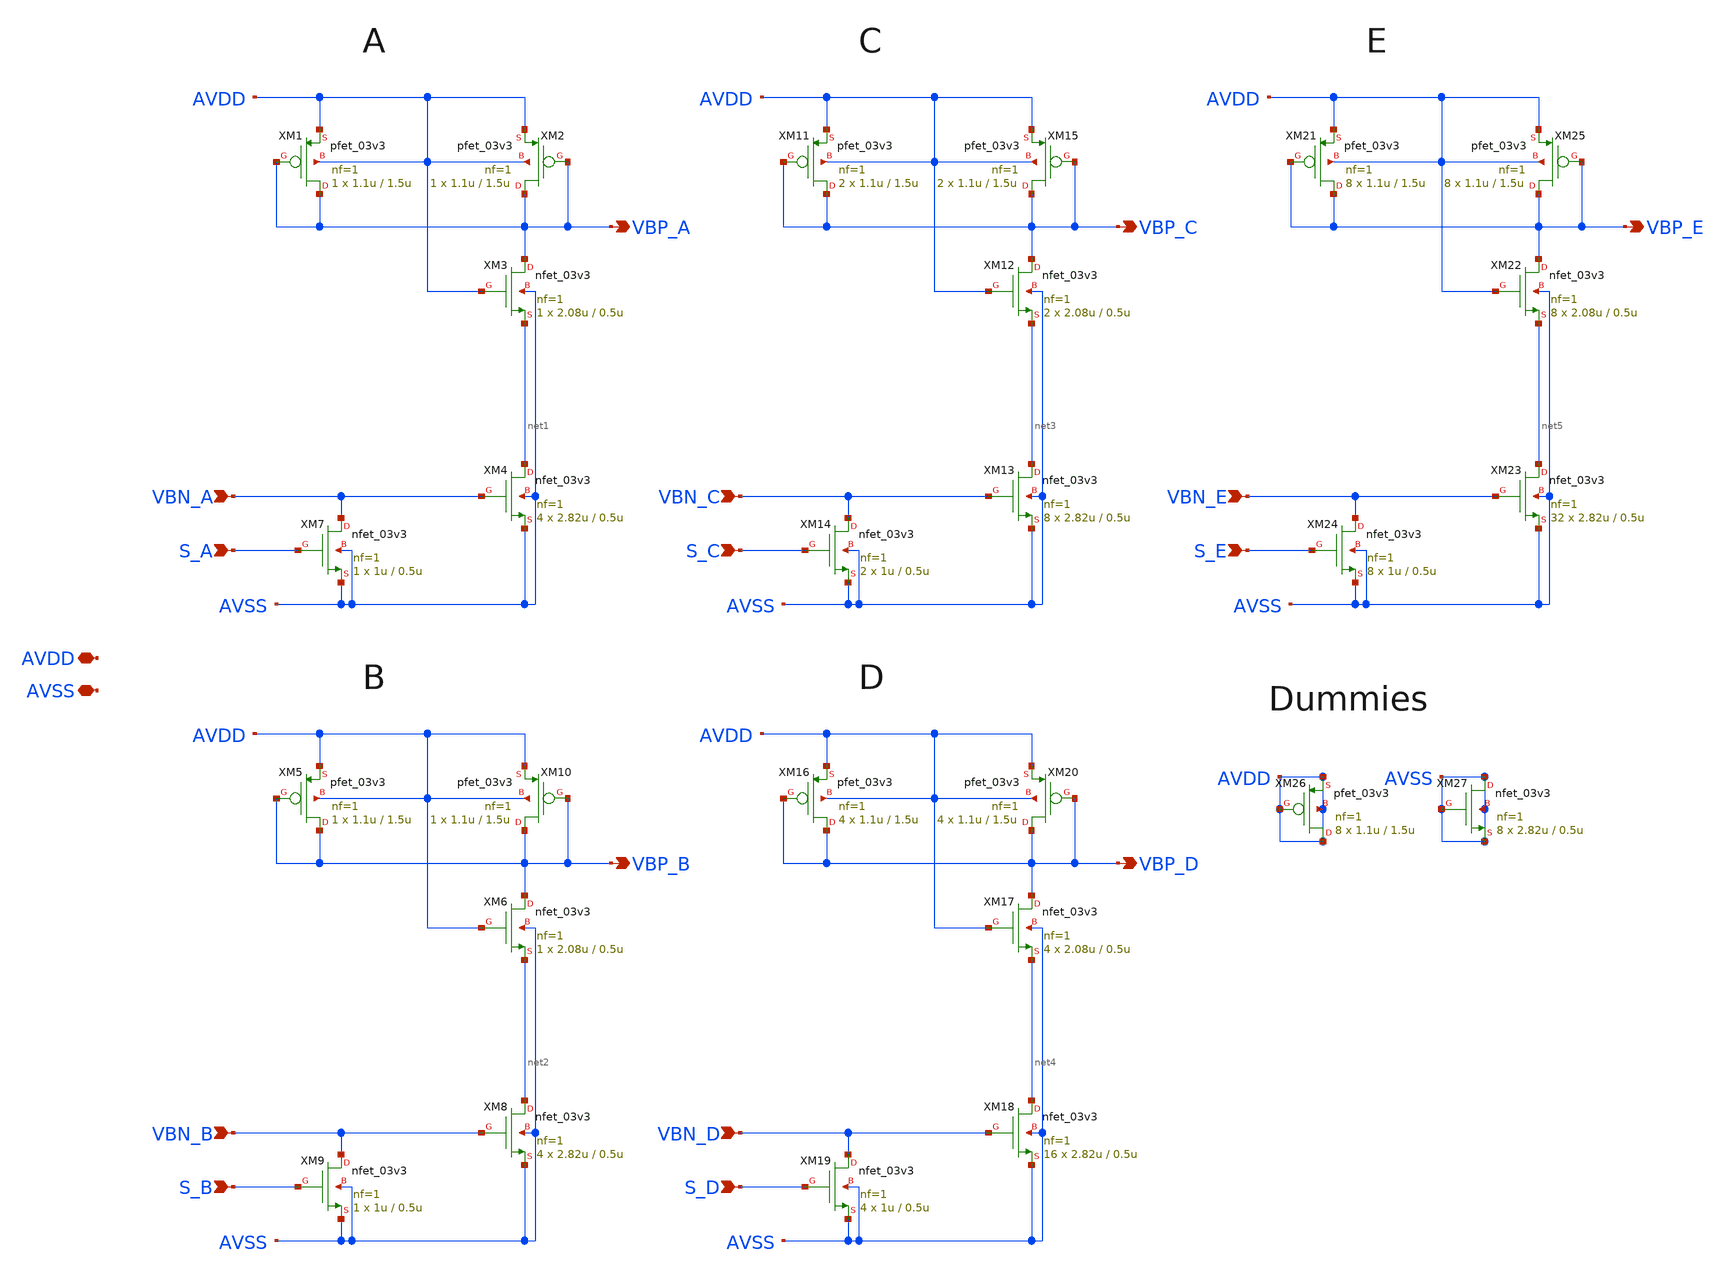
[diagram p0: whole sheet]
** sch_path: designs/libs/core_analog/feed_forward_zero/feed_forward_zero_v2_merged.sch
**.subckt feed_forward_zero_v2_merged VBP_E AVDD VBN_A VBP_A VBN_B S_B VBP_B VBN_C S_C VBP_C VBN_D
*+ S_D VBP_D VBN_E S_E S_A AVSS
*.opin VBP_E
*.iopin AVDD
*.ipin VBN_A
*.opin VBP_A
*.ipin VBN_B
*.ipin S_B
*.opin VBP_B
*.ipin VBN_C
*.ipin S_C
*.opin VBP_C
*.ipin VBN_D
*.ipin S_D
*.opin VBP_D
*.ipin VBN_E
*.ipin S_E
*.ipin S_A
*.iopin AVSS
XM1 VBP_A VBP_A AVDD AVDD pfet_03v3 L=1.5u W=1.1u nf=1 ad='int((nf+1)/2) * W/nf * 0.18u' as='int((nf+2)/2) * W/nf * 0.18u'
+ pd='2*int((nf+1)/2) * (W/nf + 0.18u)' ps='2*int((nf+2)/2) * (W/nf + 0.18u)' nrd='0.18u / W' nrs='0.18u / W'
+ sa=0 sb=0 sd=0 m=1
XM3 VBP_A AVDD net1 AVSS nfet_03v3 L=0.5u W=2.08u nf=1 ad='int((nf+1)/2) * W/nf * 0.18u' as='int((nf+2)/2) * W/nf * 0.18u'
+ pd='2*int((nf+1)/2) * (W/nf + 0.18u)' ps='2*int((nf+2)/2) * (W/nf + 0.18u)' nrd='0.18u / W' nrs='0.18u / W'
+ sa=0 sb=0 sd=0 m=1
XM4 net1 VBN_A AVSS AVSS nfet_03v3 L=0.5u W=2.82u nf=1 ad='int((nf+1)/2) * W/nf * 0.18u' as='int((nf+2)/2) * W/nf * 0.18u'
+ pd='2*int((nf+1)/2) * (W/nf + 0.18u)' ps='2*int((nf+2)/2) * (W/nf + 0.18u)' nrd='0.18u / W' nrs='0.18u / W'
+ sa=0 sb=0 sd=0 m=4
XM7 VBN_A S_A AVSS AVSS nfet_03v3 L=0.5u W=1u nf=1 ad='int((nf+1)/2) * W/nf * 0.18u' as='int((nf+2)/2) * W/nf * 0.18u'
+ pd='2*int((nf+1)/2) * (W/nf + 0.18u)' ps='2*int((nf+2)/2) * (W/nf + 0.18u)' nrd='0.18u / W' nrs='0.18u / W'
+ sa=0 sb=0 sd=0 m=1
XM2 VBP_A VBP_A AVDD AVDD pfet_03v3 L=1.5u W=1.1u nf=1 ad='int((nf+1)/2) * W/nf * 0.18u' as='int((nf+2)/2) * W/nf * 0.18u'
+ pd='2*int((nf+1)/2) * (W/nf + 0.18u)' ps='2*int((nf+2)/2) * (W/nf + 0.18u)' nrd='0.18u / W' nrs='0.18u / W'
+ sa=0 sb=0 sd=0 m=1
XM5 VBP_B VBP_B AVDD AVDD pfet_03v3 L=1.5u W=1.1u nf=1 ad='int((nf+1)/2) * W/nf * 0.18u' as='int((nf+2)/2) * W/nf * 0.18u'
+ pd='2*int((nf+1)/2) * (W/nf + 0.18u)' ps='2*int((nf+2)/2) * (W/nf + 0.18u)' nrd='0.18u / W' nrs='0.18u / W'
+ sa=0 sb=0 sd=0 m=1
XM6 VBP_B AVDD net2 AVSS nfet_03v3 L=0.5u W=2.08u nf=1 ad='int((nf+1)/2) * W/nf * 0.18u' as='int((nf+2)/2) * W/nf * 0.18u'
+ pd='2*int((nf+1)/2) * (W/nf + 0.18u)' ps='2*int((nf+2)/2) * (W/nf + 0.18u)' nrd='0.18u / W' nrs='0.18u / W'
+ sa=0 sb=0 sd=0 m=1
XM8 net2 VBN_B AVSS AVSS nfet_03v3 L=0.5u W=2.82u nf=1 ad='int((nf+1)/2) * W/nf * 0.18u' as='int((nf+2)/2) * W/nf * 0.18u'
+ pd='2*int((nf+1)/2) * (W/nf + 0.18u)' ps='2*int((nf+2)/2) * (W/nf + 0.18u)' nrd='0.18u / W' nrs='0.18u / W'
+ sa=0 sb=0 sd=0 m=4
XM9 VBN_B S_B AVSS AVSS nfet_03v3 L=0.5u W=1u nf=1 ad='int((nf+1)/2) * W/nf * 0.18u' as='int((nf+2)/2) * W/nf * 0.18u'
+ pd='2*int((nf+1)/2) * (W/nf + 0.18u)' ps='2*int((nf+2)/2) * (W/nf + 0.18u)' nrd='0.18u / W' nrs='0.18u / W'
+ sa=0 sb=0 sd=0 m=1
XM10 VBP_B VBP_B AVDD AVDD pfet_03v3 L=1.5u W=1.1u nf=1 ad='int((nf+1)/2) * W/nf * 0.18u' as='int((nf+2)/2) * W/nf * 0.18u'
+ pd='2*int((nf+1)/2) * (W/nf + 0.18u)' ps='2*int((nf+2)/2) * (W/nf + 0.18u)' nrd='0.18u / W' nrs='0.18u / W'
+ sa=0 sb=0 sd=0 m=1
XM11 VBP_C VBP_C AVDD AVDD pfet_03v3 L=1.5u W=1.1u nf=1 ad='int((nf+1)/2) * W/nf * 0.18u' as='int((nf+2)/2) * W/nf * 0.18u'
+ pd='2*int((nf+1)/2) * (W/nf + 0.18u)' ps='2*int((nf+2)/2) * (W/nf + 0.18u)' nrd='0.18u / W' nrs='0.18u / W'
+ sa=0 sb=0 sd=0 m=2
XM12 VBP_C AVDD net3 AVSS nfet_03v3 L=0.5u W=2.08u nf=1 ad='int((nf+1)/2) * W/nf * 0.18u' as='int((nf+2)/2) * W/nf * 0.18u'
+ pd='2*int((nf+1)/2) * (W/nf + 0.18u)' ps='2*int((nf+2)/2) * (W/nf + 0.18u)' nrd='0.18u / W' nrs='0.18u / W'
+ sa=0 sb=0 sd=0 m=2
XM13 net3 VBN_C AVSS AVSS nfet_03v3 L=0.5u W=2.82u nf=1 ad='int((nf+1)/2) * W/nf * 0.18u' as='int((nf+2)/2) * W/nf * 0.18u'
+ pd='2*int((nf+1)/2) * (W/nf + 0.18u)' ps='2*int((nf+2)/2) * (W/nf + 0.18u)' nrd='0.18u / W' nrs='0.18u / W'
+ sa=0 sb=0 sd=0 m=8
XM14 VBN_C S_C AVSS AVSS nfet_03v3 L=0.5u W=1u nf=1 ad='int((nf+1)/2) * W/nf * 0.18u' as='int((nf+2)/2) * W/nf * 0.18u'
+ pd='2*int((nf+1)/2) * (W/nf + 0.18u)' ps='2*int((nf+2)/2) * (W/nf + 0.18u)' nrd='0.18u / W' nrs='0.18u / W'
+ sa=0 sb=0 sd=0 m=2
XM15 VBP_C VBP_C AVDD AVDD pfet_03v3 L=1.5u W=1.1u nf=1 ad='int((nf+1)/2) * W/nf * 0.18u' as='int((nf+2)/2) * W/nf * 0.18u'
+ pd='2*int((nf+1)/2) * (W/nf + 0.18u)' ps='2*int((nf+2)/2) * (W/nf + 0.18u)' nrd='0.18u / W' nrs='0.18u / W'
+ sa=0 sb=0 sd=0 m=2
XM16 VBP_D VBP_D AVDD AVDD pfet_03v3 L=1.5u W=1.1u nf=1 ad='int((nf+1)/2) * W/nf * 0.18u' as='int((nf+2)/2) * W/nf * 0.18u'
+ pd='2*int((nf+1)/2) * (W/nf + 0.18u)' ps='2*int((nf+2)/2) * (W/nf + 0.18u)' nrd='0.18u / W' nrs='0.18u / W'
+ sa=0 sb=0 sd=0 m=4
XM17 VBP_D AVDD net4 AVSS nfet_03v3 L=0.5u W=2.08u nf=1 ad='int((nf+1)/2) * W/nf * 0.18u' as='int((nf+2)/2) * W/nf * 0.18u'
+ pd='2*int((nf+1)/2) * (W/nf + 0.18u)' ps='2*int((nf+2)/2) * (W/nf + 0.18u)' nrd='0.18u / W' nrs='0.18u / W'
+ sa=0 sb=0 sd=0 m=4
XM18 net4 VBN_D AVSS AVSS nfet_03v3 L=0.5u W=2.82u nf=1 ad='int((nf+1)/2) * W/nf * 0.18u' as='int((nf+2)/2) * W/nf * 0.18u'
+ pd='2*int((nf+1)/2) * (W/nf + 0.18u)' ps='2*int((nf+2)/2) * (W/nf + 0.18u)' nrd='0.18u / W' nrs='0.18u / W'
+ sa=0 sb=0 sd=0 m=16
XM19 VBN_D S_D AVSS AVSS nfet_03v3 L=0.5u W=1u nf=1 ad='int((nf+1)/2) * W/nf * 0.18u' as='int((nf+2)/2) * W/nf * 0.18u'
+ pd='2*int((nf+1)/2) * (W/nf + 0.18u)' ps='2*int((nf+2)/2) * (W/nf + 0.18u)' nrd='0.18u / W' nrs='0.18u / W'
+ sa=0 sb=0 sd=0 m=4
XM20 VBP_D VBP_D AVDD AVDD pfet_03v3 L=1.5u W=1.1u nf=1 ad='int((nf+1)/2) * W/nf * 0.18u' as='int((nf+2)/2) * W/nf * 0.18u'
+ pd='2*int((nf+1)/2) * (W/nf + 0.18u)' ps='2*int((nf+2)/2) * (W/nf + 0.18u)' nrd='0.18u / W' nrs='0.18u / W'
+ sa=0 sb=0 sd=0 m=4
XM21 VBP_E VBP_E AVDD AVDD pfet_03v3 L=1.5u W=1.1u nf=1 ad='int((nf+1)/2) * W/nf * 0.18u' as='int((nf+2)/2) * W/nf * 0.18u'
+ pd='2*int((nf+1)/2) * (W/nf + 0.18u)' ps='2*int((nf+2)/2) * (W/nf + 0.18u)' nrd='0.18u / W' nrs='0.18u / W'
+ sa=0 sb=0 sd=0 m=8
XM22 VBP_E AVDD net5 AVSS nfet_03v3 L=0.5u W=2.08u nf=1 ad='int((nf+1)/2) * W/nf * 0.18u' as='int((nf+2)/2) * W/nf * 0.18u'
+ pd='2*int((nf+1)/2) * (W/nf + 0.18u)' ps='2*int((nf+2)/2) * (W/nf + 0.18u)' nrd='0.18u / W' nrs='0.18u / W'
+ sa=0 sb=0 sd=0 m=8
XM23 net5 VBN_E AVSS AVSS nfet_03v3 L=0.5u W=2.82u nf=1 ad='int((nf+1)/2) * W/nf * 0.18u' as='int((nf+2)/2) * W/nf * 0.18u'
+ pd='2*int((nf+1)/2) * (W/nf + 0.18u)' ps='2*int((nf+2)/2) * (W/nf + 0.18u)' nrd='0.18u / W' nrs='0.18u / W'
+ sa=0 sb=0 sd=0 m=32
XM24 VBN_E S_E AVSS AVSS nfet_03v3 L=0.5u W=1u nf=1 ad='int((nf+1)/2) * W/nf * 0.18u' as='int((nf+2)/2) * W/nf * 0.18u'
+ pd='2*int((nf+1)/2) * (W/nf + 0.18u)' ps='2*int((nf+2)/2) * (W/nf + 0.18u)' nrd='0.18u / W' nrs='0.18u / W'
+ sa=0 sb=0 sd=0 m=8
XM25 VBP_E VBP_E AVDD AVDD pfet_03v3 L=1.5u W=1.1u nf=1 ad='int((nf+1)/2) * W/nf * 0.18u' as='int((nf+2)/2) * W/nf * 0.18u'
+ pd='2*int((nf+1)/2) * (W/nf + 0.18u)' ps='2*int((nf+2)/2) * (W/nf + 0.18u)' nrd='0.18u / W' nrs='0.18u / W'
+ sa=0 sb=0 sd=0 m=8
XM26 AVDD AVDD AVDD AVDD pfet_03v3 L=1.5u W=1.1u nf=1 ad='int((nf+1)/2) * W/nf * 0.18u' as='int((nf+2)/2) * W/nf * 0.18u'
+ pd='2*int((nf+1)/2) * (W/nf + 0.18u)' ps='2*int((nf+2)/2) * (W/nf + 0.18u)' nrd='0.18u / W' nrs='0.18u / W'
+ sa=0 sb=0 sd=0 m=8
XM27 AVSS AVSS AVSS AVSS nfet_03v3 L=0.5u W=2.82u nf=1 ad='int((nf+1)/2) * W/nf * 0.18u' as='int((nf+2)/2) * W/nf * 0.18u'
+ pd='2*int((nf+1)/2) * (W/nf + 0.18u)' ps='2*int((nf+2)/2) * (W/nf + 0.18u)' nrd='0.18u / W' nrs='0.18u / W'
+ sa=0 sb=0 sd=0 m=8
**.ends
.end
